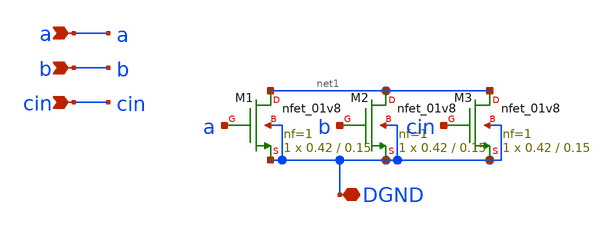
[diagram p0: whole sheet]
** sch_path: tut6/incr/fa.sch
**.subckt fa a b cin DGND
*.ipin a
*.ipin b
*.ipin cin
*.iopin DGND
XM1 net1 a DGND DGND sky130_fd_pr__nfet_01v8 L=0.15 W=0.42 nf=1 ad='int((nf+1)/2) * W/nf * 0.29' as='int((nf+2)/2) * W/nf * 0.29'
+ pd='2*int((nf+1)/2) * (W/nf + 0.29)' ps='2*int((nf+2)/2) * (W/nf + 0.29)' nrd='0.29 / W' nrs='0.29 / W'
+ sa=0 sb=0 sd=0 mult=1 m=1
XM2 net1 b DGND DGND sky130_fd_pr__nfet_01v8 L=0.15 W=0.42 nf=1 ad='int((nf+1)/2) * W/nf * 0.29' as='int((nf+2)/2) * W/nf * 0.29'
+ pd='2*int((nf+1)/2) * (W/nf + 0.29)' ps='2*int((nf+2)/2) * (W/nf + 0.29)' nrd='0.29 / W' nrs='0.29 / W'
+ sa=0 sb=0 sd=0 mult=1 m=1
XM3 net1 cin DGND DGND sky130_fd_pr__nfet_01v8 L=0.15 W=0.42 nf=1 ad='int((nf+1)/2) * W/nf * 0.29' as='int((nf+2)/2) * W/nf * 0.29'
+ pd='2*int((nf+1)/2) * (W/nf + 0.29)' ps='2*int((nf+2)/2) * (W/nf + 0.29)' nrd='0.29 / W' nrs='0.29 / W'
+ sa=0 sb=0 sd=0 mult=1 m=1
**.ends
.end
